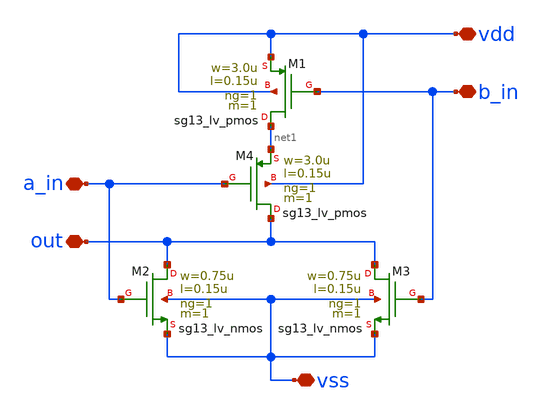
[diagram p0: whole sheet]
** sch_path: design/blocks/norgate/schematic/norgate.sch
**.subckt norgate a_in out vss vdd b_in
*.iopin a_in
*.iopin out
*.iopin vss
*.iopin vdd
*.iopin b_in
XM1 net1 b_in vdd vdd sg13_lv_pmos w=3.0u l=0.15u ng=1 m=1 mm_ok=1
XM2 out a_in vss vss sg13_lv_nmos w=0.75u l=0.15u ng=1 m=1 mm_ok=1
XM3 out b_in vss vss sg13_lv_nmos w=0.75u l=0.15u ng=1 m=1 mm_ok=1
XM4 out a_in net1 vdd sg13_lv_pmos w=3.0u l=0.15u ng=1 m=1 mm_ok=1
**.ends
.end
